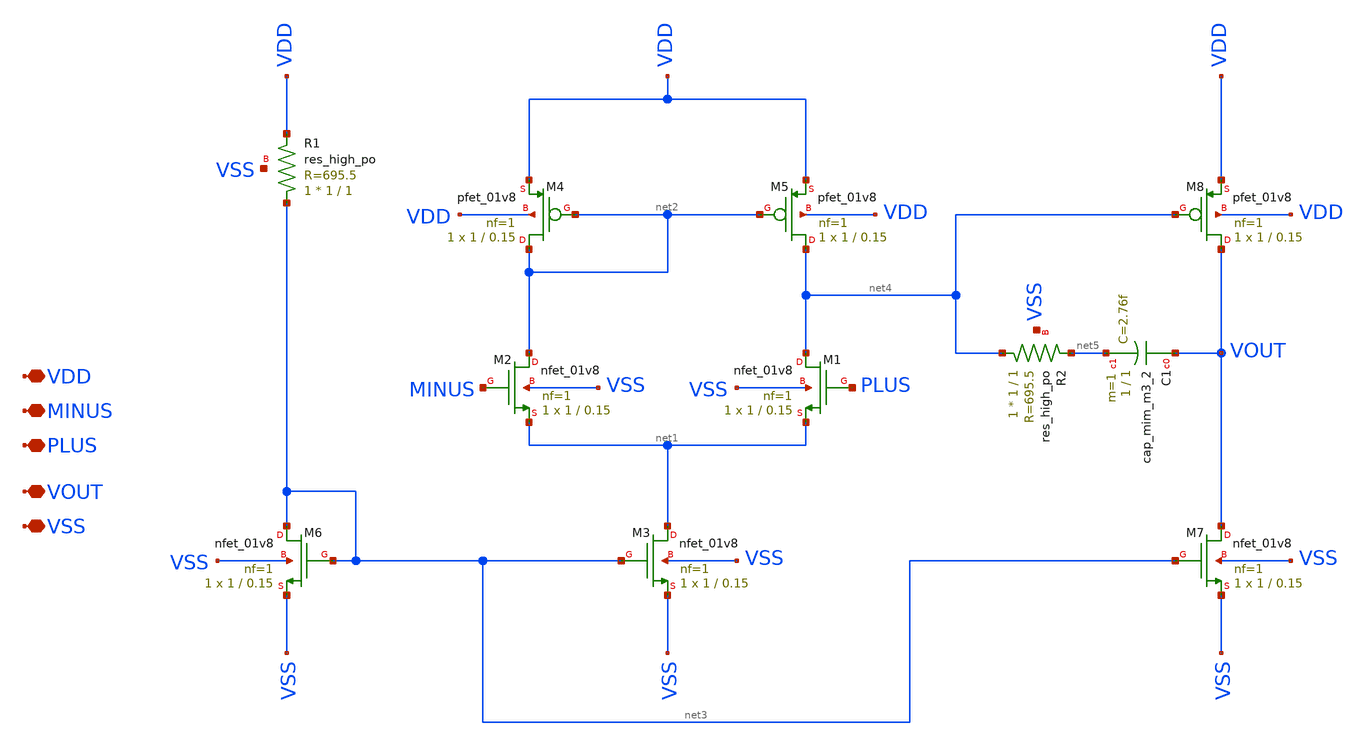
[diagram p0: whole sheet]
** sch_path: xschem/p1_opamp.sch
**.subckt p1_opamp VDD VSS PLUS MINUS VOUT
*.iopin VDD
*.iopin VSS
*.iopin PLUS
*.iopin MINUS
*.iopin VOUT
XM2 net2 MINUS net1 VSS sky130_fd_pr__nfet_01v8 L=0.15 W=1 nf=1 ad='int((nf+1)/2) * W/nf * 0.29' as='int((nf+2)/2) * W/nf * 0.29'
+ pd='2*int((nf+1)/2) * (W/nf + 0.29)' ps='2*int((nf+2)/2) * (W/nf + 0.29)' nrd='0.29 / W' nrs='0.29 / W'
+ sa=0 sb=0 sd=0 mult=1 m=1
XM1 net4 PLUS net1 VSS sky130_fd_pr__nfet_01v8 L=0.15 W=1 nf=1 ad='int((nf+1)/2) * W/nf * 0.29' as='int((nf+2)/2) * W/nf * 0.29'
+ pd='2*int((nf+1)/2) * (W/nf + 0.29)' ps='2*int((nf+2)/2) * (W/nf + 0.29)' nrd='0.29 / W' nrs='0.29 / W'
+ sa=0 sb=0 sd=0 mult=1 m=1
XM3 net1 net3 VSS VSS sky130_fd_pr__nfet_01v8 L=0.15 W=1 nf=1 ad='int((nf+1)/2) * W/nf * 0.29' as='int((nf+2)/2) * W/nf * 0.29'
+ pd='2*int((nf+1)/2) * (W/nf + 0.29)' ps='2*int((nf+2)/2) * (W/nf + 0.29)' nrd='0.29 / W' nrs='0.29 / W'
+ sa=0 sb=0 sd=0 mult=1 m=1
XM4 net2 net2 VDD VDD sky130_fd_pr__pfet_01v8 L=0.15 W=1 nf=1 ad='int((nf+1)/2) * W/nf * 0.29' as='int((nf+2)/2) * W/nf * 0.29'
+ pd='2*int((nf+1)/2) * (W/nf + 0.29)' ps='2*int((nf+2)/2) * (W/nf + 0.29)' nrd='0.29 / W' nrs='0.29 / W'
+ sa=0 sb=0 sd=0 mult=1 m=1
XM5 net4 net2 VDD VDD sky130_fd_pr__pfet_01v8 L=0.15 W=1 nf=1 ad='int((nf+1)/2) * W/nf * 0.29' as='int((nf+2)/2) * W/nf * 0.29'
+ pd='2*int((nf+1)/2) * (W/nf + 0.29)' ps='2*int((nf+2)/2) * (W/nf + 0.29)' nrd='0.29 / W' nrs='0.29 / W'
+ sa=0 sb=0 sd=0 mult=1 m=1
XM6 net3 net3 VSS VSS sky130_fd_pr__nfet_01v8 L=0.15 W=1 nf=1 ad='int((nf+1)/2) * W/nf * 0.29' as='int((nf+2)/2) * W/nf * 0.29'
+ pd='2*int((nf+1)/2) * (W/nf + 0.29)' ps='2*int((nf+2)/2) * (W/nf + 0.29)' nrd='0.29 / W' nrs='0.29 / W'
+ sa=0 sb=0 sd=0 mult=1 m=1
XR1 net3 VDD VSS sky130_fd_pr__res_high_po W=1 L=1 mult=1 m=1
XM7 VOUT net3 VSS VSS sky130_fd_pr__nfet_01v8 L=0.15 W=1 nf=1 ad='int((nf+1)/2) * W/nf * 0.29' as='int((nf+2)/2) * W/nf * 0.29'
+ pd='2*int((nf+1)/2) * (W/nf + 0.29)' ps='2*int((nf+2)/2) * (W/nf + 0.29)' nrd='0.29 / W' nrs='0.29 / W'
+ sa=0 sb=0 sd=0 mult=1 m=1
XM8 VOUT net4 VDD VDD sky130_fd_pr__pfet_01v8 L=0.15 W=1 nf=1 ad='int((nf+1)/2) * W/nf * 0.29' as='int((nf+2)/2) * W/nf * 0.29'
+ pd='2*int((nf+1)/2) * (W/nf + 0.29)' ps='2*int((nf+2)/2) * (W/nf + 0.29)' nrd='0.29 / W' nrs='0.29 / W'
+ sa=0 sb=0 sd=0 mult=1 m=1
XR2 net4 net5 VSS sky130_fd_pr__res_high_po W=1 L=1 mult=1 m=1
XC1 VOUT net5 sky130_fd_pr__cap_mim_m3_2 W=1 L=1 MF=1 m=1
**.ends
.end
